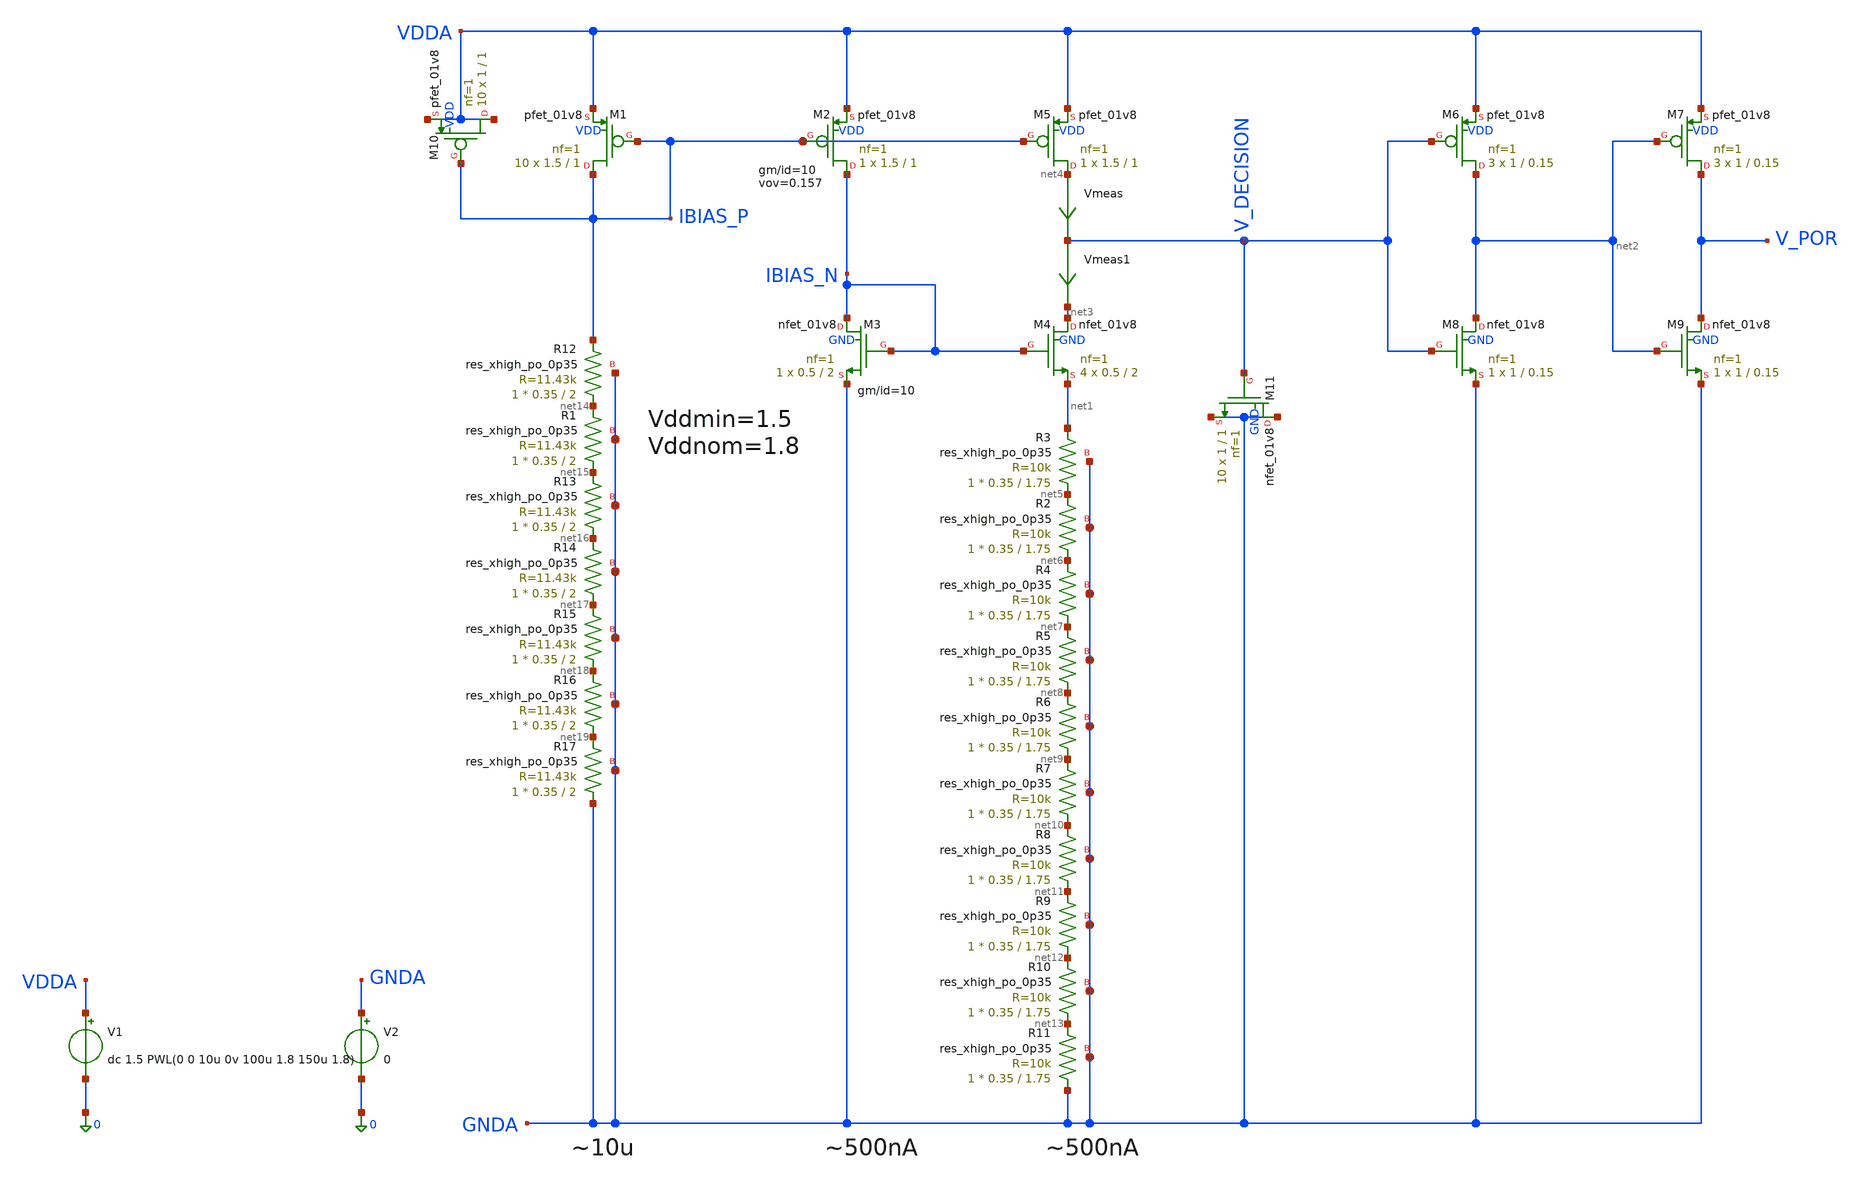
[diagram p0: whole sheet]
** sch_path: POR_V2/SKY130_POR_v1.sch
**.subckt SKY130_POR_v1
XM1 IBIAS_P IBIAS_P VDDA VDD sky130_fd_pr__pfet_01v8 L=1 W=1.5 nf=1 ad='int((1 + 1)/2) * 1.5 / 1 * 0.29'
+ as='int((1 + 2)/2) * 1.5 / 1 * 0.29' pd='2*int((1 + 1)/2) * (1.5 / 1 + 0.29)' ps='2*int((1 + 2)/2) * (1.5 / 1 + 0.29)'
+ nrd='0.29 / 1.5 ' nrs='0.29 / 1.5 ' sa=0 sb=0 sd=0 mult=10 m=10
XM2 IBIAS_N IBIAS_P VDDA VDD sky130_fd_pr__pfet_01v8 L=1 W=1.5 nf=1 ad='int((1 + 1)/2) * 1.5 / 1 * 0.29'
+ as='int((1 + 2)/2) * 1.5 / 1 * 0.29' pd='2*int((1 + 1)/2) * (1.5 / 1 + 0.29)' ps='2*int((1 + 2)/2) * (1.5 / 1 + 0.29)'
+ nrd='0.29 / 1.5 ' nrs='0.29 / 1.5 ' sa=0 sb=0 sd=0 mult=1 m=1
XM3 IBIAS_N IBIAS_N GNDA GND sky130_fd_pr__nfet_01v8 L=2 W=0.5 nf=1 ad='int((1 + 1)/2) * 0.5 / 1 * 0.29'
+ as='int((1 + 2)/2) * 0.5 / 1 * 0.29' pd='2*int((1 + 1)/2) * (0.5 / 1 + 0.29)' ps='2*int((1 + 2)/2) * (0.5 / 1 + 0.29)'
+ nrd='0.29 / 0.5 ' nrs='0.29 / 0.5 ' sa=0 sb=0 sd=0 mult=1 m=1
XM4 net3 IBIAS_N net1 GND sky130_fd_pr__nfet_01v8 L=2 W=0.5 nf=1 ad='int((1 + 1)/2) * 0.5 / 1 * 0.29'
+ as='int((1 + 2)/2) * 0.5 / 1 * 0.29' pd='2*int((1 + 1)/2) * (0.5 / 1 + 0.29)' ps='2*int((1 + 2)/2) * (0.5 / 1 + 0.29)'
+ nrd='0.29 / 0.5 ' nrs='0.29 / 0.5 ' sa=0 sb=0 sd=0 mult=4 m=4
XM5 net4 IBIAS_P VDDA VDD sky130_fd_pr__pfet_01v8 L=1 W=1.5 nf=1 ad='int((1 + 1)/2) * 1.5 / 1 * 0.29'
+ as='int((1 + 2)/2) * 1.5 / 1 * 0.29' pd='2*int((1 + 1)/2) * (1.5 / 1 + 0.29)' ps='2*int((1 + 2)/2) * (1.5 / 1 + 0.29)'
+ nrd='0.29 / 1.5 ' nrs='0.29 / 1.5 ' sa=0 sb=0 sd=0 mult=1 m=1
XM6 net2 V_DECISION VDDA VDD sky130_fd_pr__pfet_01v8 L=0.15 W=1 nf=1 ad='int((1 + 1)/2) * 1 / 1 * 0.29'
+ as='int((1 + 2)/2) * 1 / 1 * 0.29' pd='2*int((1 + 1)/2) * (1 / 1 + 0.29)' ps='2*int((1 + 2)/2) * (1 / 1 + 0.29)'
+ nrd='0.29 / 1 ' nrs='0.29 / 1 ' sa=0 sb=0 sd=0 mult=3 m=3
XM8 net2 V_DECISION GNDA GND sky130_fd_pr__nfet_01v8 L=0.15 W=1 nf=1 ad='int((1 + 1)/2) * 1 / 1 * 0.29'
+ as='int((1 + 2)/2) * 1 / 1 * 0.29' pd='2*int((1 + 1)/2) * (1 / 1 + 0.29)' ps='2*int((1 + 2)/2) * (1 / 1 + 0.29)'
+ nrd='0.29 / 1 ' nrs='0.29 / 1 ' sa=0 sb=0 sd=0 mult=1 m=1
XM7 V_POR net2 VDDA VDD sky130_fd_pr__pfet_01v8 L=0.15 W=1 nf=1 ad='int((1 + 1)/2) * 1 / 1 * 0.29' as='int((1 + 2)/2) * 1 / 1 * 0.29'
+ pd='2*int((1 + 1)/2) * (1 / 1 + 0.29)' ps='2*int((1 + 2)/2) * (1 / 1 + 0.29)' nrd='0.29 / 1 ' nrs='0.29 / 1 '
+ sa=0 sb=0 sd=0 mult=3 m=3
XM9 V_POR net2 GNDA GND sky130_fd_pr__nfet_01v8 L=0.15 W=1 nf=1 ad='int((1 + 1)/2) * 1 / 1 * 0.29' as='int((1 + 2)/2) * 1 / 1 * 0.29'
+ pd='2*int((1 + 1)/2) * (1 / 1 + 0.29)' ps='2*int((1 + 2)/2) * (1 / 1 + 0.29)' nrd='0.29 / 1 ' nrs='0.29 / 1 '
+ sa=0 sb=0 sd=0 mult=1 m=1
V1 VDDA 0 dc 1.5 PWL(0 0 10u 0v 100u 1.8 150u 1.8)
V2 GNDA 0 0
XM10 VDDA IBIAS_P VDDA VDD sky130_fd_pr__pfet_01v8 L=1 W=1 nf=1 ad='int((1 + 1)/2) * 1 / 1 * 0.29' as='int((1 + 2)/2) * 1 / 1 * 0.29'
+ pd='2*int((1 + 1)/2) * (1 / 1 + 0.29)' ps='2*int((1 + 2)/2) * (1 / 1 + 0.29)' nrd='0.29 / 1 ' nrs='0.29 / 1 '
+ sa=0 sb=0 sd=0 mult=10 m=10
XM11 GNDA V_DECISION GNDA GND sky130_fd_pr__nfet_01v8 L=1 W=1 nf=1 ad='int((1 + 1)/2) * 1 / 1 * 0.29'
+ as='int((1 + 2)/2) * 1 / 1 * 0.29' pd='2*int((1 + 1)/2) * (1 / 1 + 0.29)' ps='2*int((1 + 2)/2) * (1 / 1 + 0.29)'
+ nrd='0.29 / 1 ' nrs='0.29 / 1 ' sa=0 sb=0 sd=0 mult=10 m=10
Vmeas net4 V_DECISION 0
.save i(vmeas)
Vmeas1 V_DECISION net3 0
.save i(vmeas1)
XR3 net5 net1 GNDA sky130_fd_pr__res_xhigh_po_0p35 L=1.75 mult=1 m=1
XR2 net6 net5 GNDA sky130_fd_pr__res_xhigh_po_0p35 L=1.75 mult=1 m=1
XR4 net7 net6 GNDA sky130_fd_pr__res_xhigh_po_0p35 L=1.75 mult=1 m=1
XR5 net8 net7 GNDA sky130_fd_pr__res_xhigh_po_0p35 L=1.75 mult=1 m=1
XR6 net9 net8 GNDA sky130_fd_pr__res_xhigh_po_0p35 L=1.75 mult=1 m=1
XR7 net10 net9 GNDA sky130_fd_pr__res_xhigh_po_0p35 L=1.75 mult=1 m=1
XR8 net11 net10 GNDA sky130_fd_pr__res_xhigh_po_0p35 L=1.75 mult=1 m=1
XR9 net12 net11 GNDA sky130_fd_pr__res_xhigh_po_0p35 L=1.75 mult=1 m=1
XR10 net13 net12 GNDA sky130_fd_pr__res_xhigh_po_0p35 L=1.75 mult=1 m=1
XR11 GNDA net13 GNDA sky130_fd_pr__res_xhigh_po_0p35 L=1.75 mult=1 m=1
XR12 net14 IBIAS_P GNDA sky130_fd_pr__res_xhigh_po_0p35 L=2 mult=1 m=1
XR1 net15 net14 GNDA sky130_fd_pr__res_xhigh_po_0p35 L=2 mult=1 m=1
XR13 net16 net15 GNDA sky130_fd_pr__res_xhigh_po_0p35 L=2 mult=1 m=1
XR14 net17 net16 GNDA sky130_fd_pr__res_xhigh_po_0p35 L=2 mult=1 m=1
XR15 net18 net17 GNDA sky130_fd_pr__res_xhigh_po_0p35 L=2 mult=1 m=1
XR16 net19 net18 GNDA sky130_fd_pr__res_xhigh_po_0p35 L=2 mult=1 m=1
XR17 GNDA net19 GNDA sky130_fd_pr__res_xhigh_po_0p35 L=2 mult=1 m=1
**** begin user architecture code


.option wnflag=1 gmin=1e-18
.option savecurrents
.temp 27
.control
save all
op
write SKY130_POR_v1.raw
set appendwrite
dc V1 0 1.8 10m
let Idiff= vmeas#branch-vmeas1#branch
plot v(V_POR) v(V_DECISION) v(VDDA)
plot v(V_POR) vs v(VDDA)
plot v(V_DECISION) vs v(VDDA)
plot vmeas#branch vmeas1#branch
plot Idiff
write SKY130_POR_v1.raw
set appendwrite
.endc





.save @m.xm1.msky130_fd_pr__pfet_01v8[gm]
.save @m.xm1.msky130_fd_pr__pfet_01v8[gds]
.save @m.xm1.msky130_fd_pr__pfet_01v8[vth]
.save @m.xm1.msky130_fd_pr__pfet_01v8[vdsat]
.save @m.xm1.msky130_fd_pr__pfet_01v8[cgg]
.save @m.xm1.msky130_fd_pr__pfet_01v8[cgso]
.save @m.xm1.msky130_fd_pr__pfet_01v8[cgdo]
.save @m.xm2.msky130_fd_pr__pfet_01v8[gm]
.save @m.xm2.msky130_fd_pr__pfet_01v8[gds]
.save @m.xm2.msky130_fd_pr__pfet_01v8[vth]
.save @m.xm2.msky130_fd_pr__pfet_01v8[vdsat]
.save @m.xm2.msky130_fd_pr__pfet_01v8[cgg]
.save @m.xm2.msky130_fd_pr__pfet_01v8[cgso]
.save @m.xm2.msky130_fd_pr__pfet_01v8[cgdo]
.save @m.xm3.msky130_fd_pr__nfet_01v8[gm]
.save @m.xm3.msky130_fd_pr__nfet_01v8[gds]
.save @m.xm3.msky130_fd_pr__nfet_01v8[vth]
.save @m.xm3.msky130_fd_pr__nfet_01v8[vdsat]
.save @m.xm3.msky130_fd_pr__nfet_01v8[cgg]
.save @m.xm3.msky130_fd_pr__nfet_01v8[cgso]
.save @m.xm3.msky130_fd_pr__nfet_01v8[cgdo]
.save @m.xm4.msky130_fd_pr__nfet_01v8[gm]
.save @m.xm4.msky130_fd_pr__nfet_01v8[gds]
.save @m.xm4.msky130_fd_pr__nfet_01v8[vth]
.save @m.xm4.msky130_fd_pr__nfet_01v8[vdsat]
.save @m.xm4.msky130_fd_pr__nfet_01v8[cgg]
.save @m.xm4.msky130_fd_pr__nfet_01v8[cgso]
.save @m.xm4.msky130_fd_pr__nfet_01v8[cgdo]
.save @m.xm5.msky130_fd_pr__pfet_01v8[gm]
.save @m.xm5.msky130_fd_pr__pfet_01v8[gds]
.save @m.xm5.msky130_fd_pr__pfet_01v8[vth]
.save @m.xm5.msky130_fd_pr__pfet_01v8[vdsat]
.save @m.xm5.msky130_fd_pr__pfet_01v8[cgg]
.save @m.xm5.msky130_fd_pr__pfet_01v8[cgso]
.save @m.xm5.msky130_fd_pr__pfet_01v8[cgdo]
.save @m.xm6.msky130_fd_pr__pfet_01v8[gm]
.save @m.xm6.msky130_fd_pr__pfet_01v8[gds]
.save @m.xm6.msky130_fd_pr__pfet_01v8[vth]
.save @m.xm6.msky130_fd_pr__pfet_01v8[vdsat]
.save @m.xm6.msky130_fd_pr__pfet_01v8[cgg]
.save @m.xm6.msky130_fd_pr__pfet_01v8[cgso]
.save @m.xm6.msky130_fd_pr__pfet_01v8[cgdo]
.save @m.xm8.msky130_fd_pr__nfet_01v8[gm]
.save @m.xm8.msky130_fd_pr__nfet_01v8[gds]
.save @m.xm8.msky130_fd_pr__nfet_01v8[vth]
.save @m.xm8.msky130_fd_pr__nfet_01v8[vdsat]
.save @m.xm8.msky130_fd_pr__nfet_01v8[cgg]
.save @m.xm8.msky130_fd_pr__nfet_01v8[cgso]
.save @m.xm8.msky130_fd_pr__nfet_01v8[cgdo]
.save @m.xm7.msky130_fd_pr__pfet_01v8[gm]
.save @m.xm7.msky130_fd_pr__pfet_01v8[gds]
.save @m.xm7.msky130_fd_pr__pfet_01v8[vth]
.save @m.xm7.msky130_fd_pr__pfet_01v8[vdsat]
.save @m.xm7.msky130_fd_pr__pfet_01v8[cgg]
.save @m.xm7.msky130_fd_pr__pfet_01v8[cgso]
.save @m.xm7.msky130_fd_pr__pfet_01v8[cgdo]
.save @m.xm9.msky130_fd_pr__nfet_01v8[gm]
.save @m.xm9.msky130_fd_pr__nfet_01v8[gds]
.save @m.xm9.msky130_fd_pr__nfet_01v8[vth]
.save @m.xm9.msky130_fd_pr__nfet_01v8[vdsat]
.save @m.xm9.msky130_fd_pr__nfet_01v8[cgg]
.save @m.xm9.msky130_fd_pr__nfet_01v8[cgso]
.save @m.xm9.msky130_fd_pr__nfet_01v8[cgdo]
.save @m.xm10.msky130_fd_pr__pfet_01v8[gm]
.save @m.xm10.msky130_fd_pr__pfet_01v8[gds]
.save @m.xm10.msky130_fd_pr__pfet_01v8[vth]
.save @m.xm10.msky130_fd_pr__pfet_01v8[vdsat]
.save @m.xm10.msky130_fd_pr__pfet_01v8[cgg]
.save @m.xm10.msky130_fd_pr__pfet_01v8[cgso]
.save @m.xm10.msky130_fd_pr__pfet_01v8[cgdo]
.save @m.xm11.msky130_fd_pr__nfet_01v8[gm]
.save @m.xm11.msky130_fd_pr__nfet_01v8[gds]
.save @m.xm11.msky130_fd_pr__nfet_01v8[vth]
.save @m.xm11.msky130_fd_pr__nfet_01v8[vdsat]
.save @m.xm11.msky130_fd_pr__nfet_01v8[cgg]
.save @m.xm11.msky130_fd_pr__nfet_01v8[cgso]
.save @m.xm11.msky130_fd_pr__nfet_01v8[cgdo]



** opencircuitdesign pdks install
.lib $::SKYWATER_MODELS/sky130.lib.spice fs



.option wnflag=1 gmin=1e-18
.option savecurrents
.temp 27
.control
save all
op
write SKY130_POR_v1.raw
set appendwrite
tran 0.1u 150u uic
plot v(V_POR) v(V_DECISION) v(VDDA)
plot v(V_POR) vs v(VDDA)
plot v(V_DECISION) vs v(VDDA)
plot vmeas#branch vmeas1#branch
plot Idiff
write SKY130_POR_v1.raw
.endc




.option wnflag=1 gmin=1e-18
.option savecurrents
.temp 27
.control
save all
op
write SKY130_POR_v1.raw
set appendwrite
dc temp -50 150 10
let Idiff= vmeas#branch-vmeas1#branch
plot v(V_POR) v(V_DECISION) v(VDDA)
plot v(V_POR) vs v(VDDA)
plot v(V_DECISION) vs v(VDDA)
plot vmeas#branch vmeas1#branch
plot Idiff
write SKY130_POR_v1.raw
set appendwrite
.endc


**** end user architecture code
**.ends
.end
